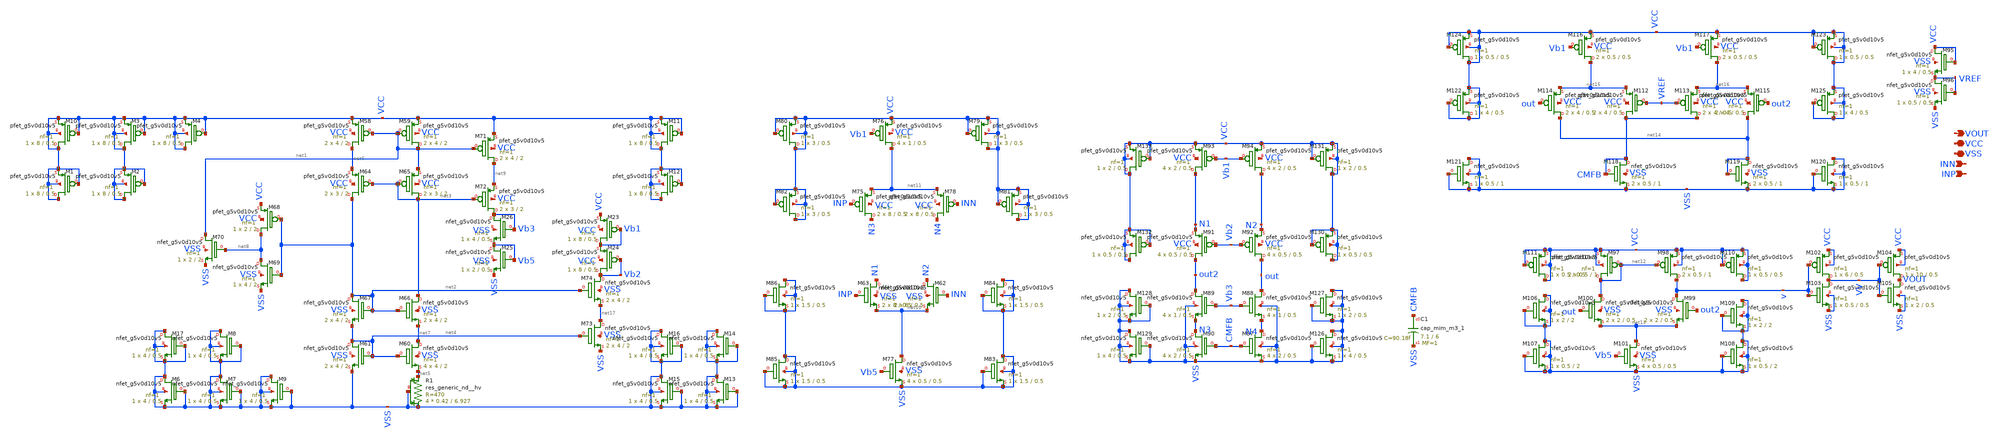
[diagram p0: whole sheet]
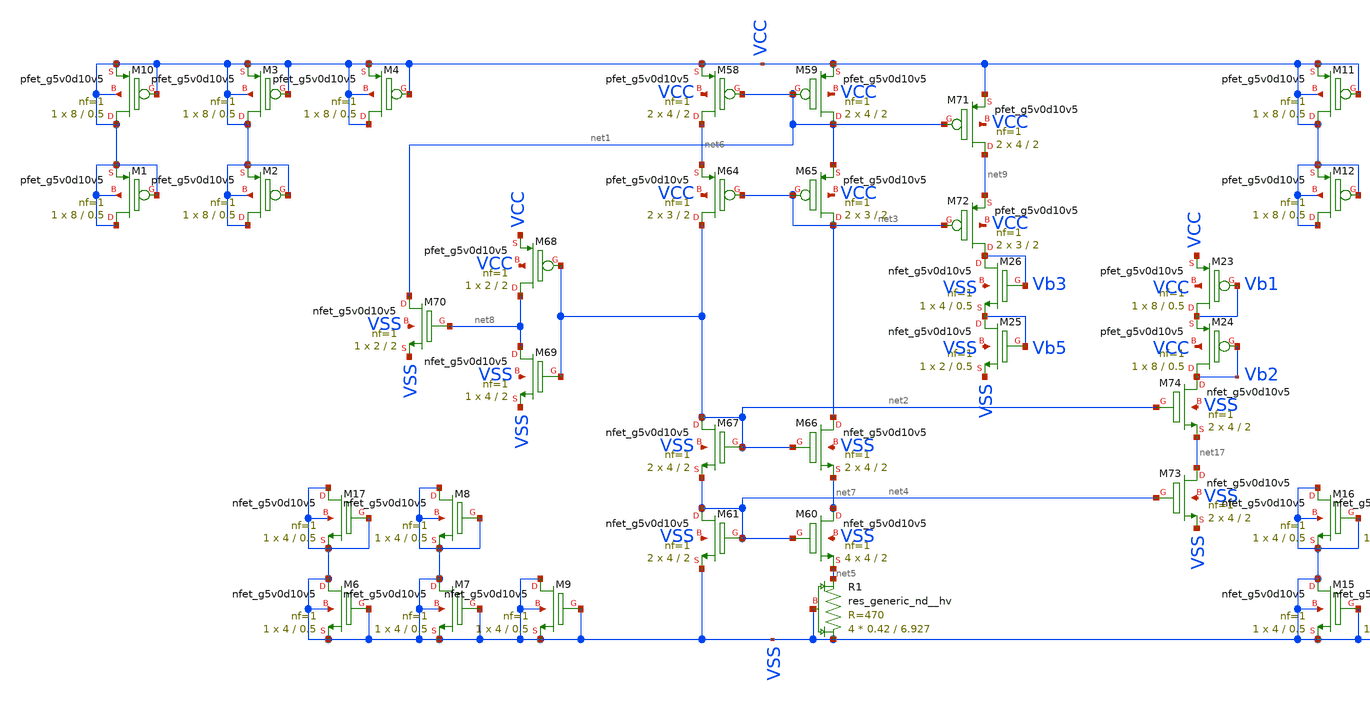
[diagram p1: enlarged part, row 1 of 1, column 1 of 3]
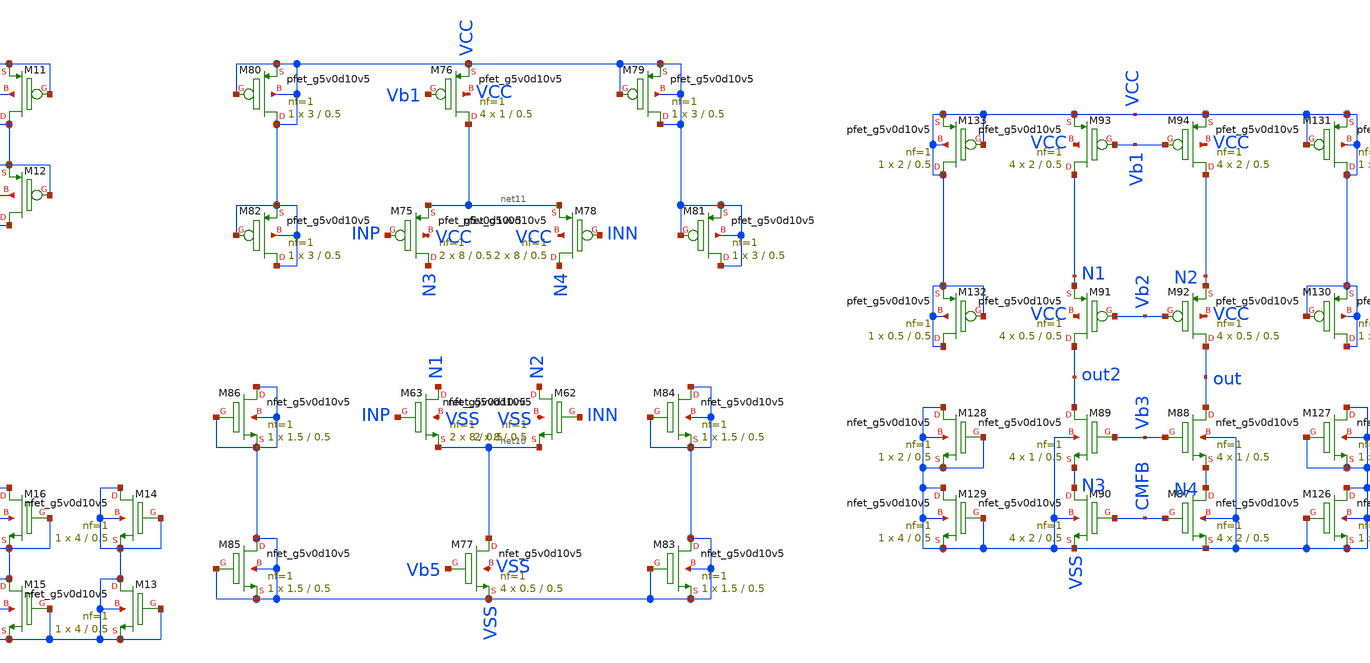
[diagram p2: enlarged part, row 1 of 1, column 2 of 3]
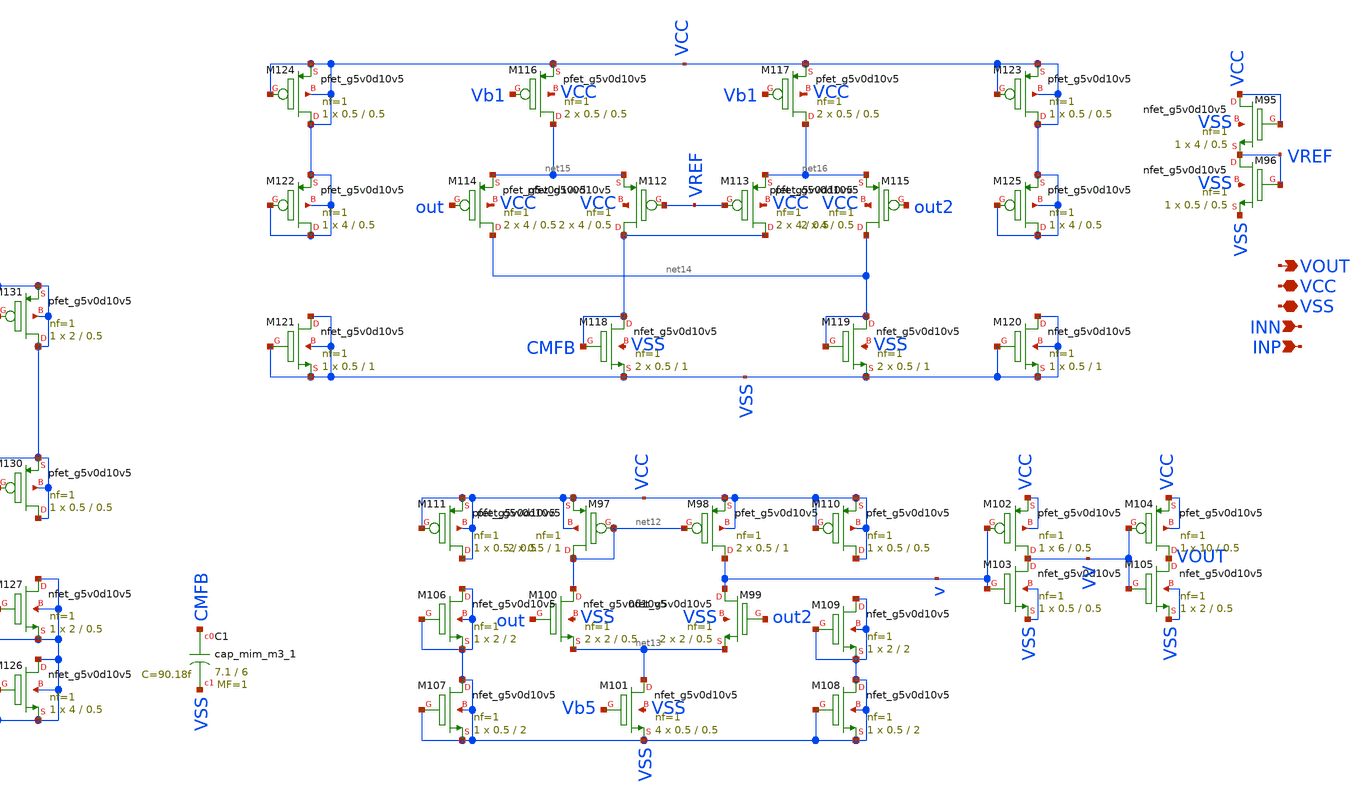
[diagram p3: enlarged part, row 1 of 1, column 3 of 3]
** sch_path: latest_working_comparator/backup_schematic/folded_cascode.sch
**.subckt folded_cascode VCC VSS INN INP VOUT
*.iopin VCC
*.iopin VSS
*.ipin INN
*.ipin INP
*.opin VOUT
XM23 Vb1 Vb1 VCC VCC sky130_fd_pr__pfet_g5v0d10v5 L=0.5 W=8 nf=1 ad='int((nf+1)/2) * W/nf * 0.29' as='int((nf+2)/2) * W/nf * 0.29'
+ pd='2*int((nf+1)/2) * (W/nf + 0.29)' ps='2*int((nf+2)/2) * (W/nf + 0.29)' nrd='0.29 / W' nrs='0.29 / W'
+ sa=0 sb=0 sd=0 mult=1 m=1
XM24 Vb2 Vb2 Vb1 VCC sky130_fd_pr__pfet_g5v0d10v5 L=0.5 W=8 nf=1 ad='int((nf+1)/2) * W/nf * 0.29' as='int((nf+2)/2) * W/nf * 0.29'
+ pd='2*int((nf+1)/2) * (W/nf + 0.29)' ps='2*int((nf+2)/2) * (W/nf + 0.29)' nrd='0.29 / W' nrs='0.29 / W'
+ sa=0 sb=0 sd=0 mult=1 m=1
XM25 Vb5 Vb5 VSS VSS sky130_fd_pr__nfet_g5v0d10v5 L=0.5 W=2 nf=1 ad='int((nf+1)/2) * W/nf * 0.29' as='int((nf+2)/2) * W/nf * 0.29'
+ pd='2*int((nf+1)/2) * (W/nf + 0.29)' ps='2*int((nf+2)/2) * (W/nf + 0.29)' nrd='0.29 / W' nrs='0.29 / W'
+ sa=0 sb=0 sd=0 mult=1 m=1
XM26 Vb3 Vb3 Vb5 VSS sky130_fd_pr__nfet_g5v0d10v5 L=0.5 W=4 nf=1 ad='int((nf+1)/2) * W/nf * 0.29' as='int((nf+2)/2) * W/nf * 0.29'
+ pd='2*int((nf+1)/2) * (W/nf + 0.29)' ps='2*int((nf+2)/2) * (W/nf + 0.29)' nrd='0.29 / W' nrs='0.29 / W'
+ sa=0 sb=0 sd=0 mult=1 m=1
XM58 net6 net1 VCC VCC sky130_fd_pr__pfet_g5v0d10v5 L=2 W=4 nf=1 ad='int((nf+1)/2) * W/nf * 0.29' as='int((nf+2)/2) * W/nf * 0.29'
+ pd='2*int((nf+1)/2) * (W/nf + 0.29)' ps='2*int((nf+2)/2) * (W/nf + 0.29)' nrd='0.29 / W' nrs='0.29 / W'
+ sa=0 sb=0 sd=0 mult=2 m=2
XM59 net1 net1 VCC VCC sky130_fd_pr__pfet_g5v0d10v5 L=2 W=4 nf=1 ad='int((nf+1)/2) * W/nf * 0.29' as='int((nf+2)/2) * W/nf * 0.29'
+ pd='2*int((nf+1)/2) * (W/nf + 0.29)' ps='2*int((nf+2)/2) * (W/nf + 0.29)' nrd='0.29 / W' nrs='0.29 / W'
+ sa=0 sb=0 sd=0 mult=2 m=2
XM60 net7 net4 net5 VSS sky130_fd_pr__nfet_g5v0d10v5 L=2 W=4 nf=1 ad='int((nf+1)/2) * W/nf * 0.29' as='int((nf+2)/2) * W/nf * 0.29'
+ pd='2*int((nf+1)/2) * (W/nf + 0.29)' ps='2*int((nf+2)/2) * (W/nf + 0.29)' nrd='0.29 / W' nrs='0.29 / W'
+ sa=0 sb=0 sd=0 mult=4 m=4
XM61 net4 net4 VSS VSS sky130_fd_pr__nfet_g5v0d10v5 L=2 W=4 nf=1 ad='int((nf+1)/2) * W/nf * 0.29' as='int((nf+2)/2) * W/nf * 0.29'
+ pd='2*int((nf+1)/2) * (W/nf + 0.29)' ps='2*int((nf+2)/2) * (W/nf + 0.29)' nrd='0.29 / W' nrs='0.29 / W'
+ sa=0 sb=0 sd=0 mult=2 m=2
XM64 net2 net3 net6 VCC sky130_fd_pr__pfet_g5v0d10v5 L=2 W=3 nf=1 ad='int((nf+1)/2) * W/nf * 0.29' as='int((nf+2)/2) * W/nf * 0.29'
+ pd='2*int((nf+1)/2) * (W/nf + 0.29)' ps='2*int((nf+2)/2) * (W/nf + 0.29)' nrd='0.29 / W' nrs='0.29 / W'
+ sa=0 sb=0 sd=0 mult=2 m=2
XM65 net3 net3 net1 VCC sky130_fd_pr__pfet_g5v0d10v5 L=2 W=3 nf=1 ad='int((nf+1)/2) * W/nf * 0.29' as='int((nf+2)/2) * W/nf * 0.29'
+ pd='2*int((nf+1)/2) * (W/nf + 0.29)' ps='2*int((nf+2)/2) * (W/nf + 0.29)' nrd='0.29 / W' nrs='0.29 / W'
+ sa=0 sb=0 sd=0 mult=2 m=2
XM66 net3 net2 net7 VSS sky130_fd_pr__nfet_g5v0d10v5 L=2 W=4 nf=1 ad='int((nf+1)/2) * W/nf * 0.29' as='int((nf+2)/2) * W/nf * 0.29'
+ pd='2*int((nf+1)/2) * (W/nf + 0.29)' ps='2*int((nf+2)/2) * (W/nf + 0.29)' nrd='0.29 / W' nrs='0.29 / W'
+ sa=0 sb=0 sd=0 mult=2 m=2
XM67 net2 net2 net4 VSS sky130_fd_pr__nfet_g5v0d10v5 L=2 W=4 nf=1 ad='int((nf+1)/2) * W/nf * 0.29' as='int((nf+2)/2) * W/nf * 0.29'
+ pd='2*int((nf+1)/2) * (W/nf + 0.29)' ps='2*int((nf+2)/2) * (W/nf + 0.29)' nrd='0.29 / W' nrs='0.29 / W'
+ sa=0 sb=0 sd=0 mult=2 m=2
XM68 net8 net2 VCC VCC sky130_fd_pr__pfet_g5v0d10v5 L=2 W=2 nf=1 ad='int((nf+1)/2) * W/nf * 0.29' as='int((nf+2)/2) * W/nf * 0.29'
+ pd='2*int((nf+1)/2) * (W/nf + 0.29)' ps='2*int((nf+2)/2) * (W/nf + 0.29)' nrd='0.29 / W' nrs='0.29 / W'
+ sa=0 sb=0 sd=0 mult=1 m=1
XM69 net8 net2 VSS VSS sky130_fd_pr__nfet_g5v0d10v5 L=2 W=4 nf=1 ad='int((nf+1)/2) * W/nf * 0.29' as='int((nf+2)/2) * W/nf * 0.29'
+ pd='2*int((nf+1)/2) * (W/nf + 0.29)' ps='2*int((nf+2)/2) * (W/nf + 0.29)' nrd='0.29 / W' nrs='0.29 / W'
+ sa=0 sb=0 sd=0 mult=1 m=1
XM70 net1 net8 VSS VSS sky130_fd_pr__nfet_g5v0d10v5 L=2 W=2 nf=1 ad='int((nf+1)/2) * W/nf * 0.29' as='int((nf+2)/2) * W/nf * 0.29'
+ pd='2*int((nf+1)/2) * (W/nf + 0.29)' ps='2*int((nf+2)/2) * (W/nf + 0.29)' nrd='0.29 / W' nrs='0.29 / W'
+ sa=0 sb=0 sd=0 mult=1 m=1
XM71 net9 net1 VCC VCC sky130_fd_pr__pfet_g5v0d10v5 L=2 W=4 nf=1 ad='int((nf+1)/2) * W/nf * 0.29' as='int((nf+2)/2) * W/nf * 0.29'
+ pd='2*int((nf+1)/2) * (W/nf + 0.29)' ps='2*int((nf+2)/2) * (W/nf + 0.29)' nrd='0.29 / W' nrs='0.29 / W'
+ sa=0 sb=0 sd=0 mult=2 m=2
XM72 Vb3 net3 net9 VCC sky130_fd_pr__pfet_g5v0d10v5 L=2 W=3 nf=1 ad='int((nf+1)/2) * W/nf * 0.29' as='int((nf+2)/2) * W/nf * 0.29'
+ pd='2*int((nf+1)/2) * (W/nf + 0.29)' ps='2*int((nf+2)/2) * (W/nf + 0.29)' nrd='0.29 / W' nrs='0.29 / W'
+ sa=0 sb=0 sd=0 mult=2 m=2
XM73 net17 net4 VSS VSS sky130_fd_pr__nfet_g5v0d10v5 L=2 W=4 nf=1 ad='int((nf+1)/2) * W/nf * 0.29' as='int((nf+2)/2) * W/nf * 0.29'
+ pd='2*int((nf+1)/2) * (W/nf + 0.29)' ps='2*int((nf+2)/2) * (W/nf + 0.29)' nrd='0.29 / W' nrs='0.29 / W'
+ sa=0 sb=0 sd=0 mult=2 m=2
XM74 Vb2 net2 net17 VSS sky130_fd_pr__nfet_g5v0d10v5 L=2 W=4 nf=1 ad='int((nf+1)/2) * W/nf * 0.29' as='int((nf+2)/2) * W/nf * 0.29'
+ pd='2*int((nf+1)/2) * (W/nf + 0.29)' ps='2*int((nf+2)/2) * (W/nf + 0.29)' nrd='0.29 / W' nrs='0.29 / W'
+ sa=0 sb=0 sd=0 mult=2 m=2
XM62 N2 INN net10 VSS sky130_fd_pr__nfet_g5v0d10v5 L=0.5 W=8 nf=1 ad='int((nf+1)/2) * W/nf * 0.29' as='int((nf+2)/2) * W/nf * 0.29'
+ pd='2*int((nf+1)/2) * (W/nf + 0.29)' ps='2*int((nf+2)/2) * (W/nf + 0.29)' nrd='0.29 / W' nrs='0.29 / W'
+ sa=0 sb=0 sd=0 mult=2 m=2
XM63 N1 INP net10 VSS sky130_fd_pr__nfet_g5v0d10v5 L=0.5 W=8 nf=1 ad='int((nf+1)/2) * W/nf * 0.29' as='int((nf+2)/2) * W/nf * 0.29'
+ pd='2*int((nf+1)/2) * (W/nf + 0.29)' ps='2*int((nf+2)/2) * (W/nf + 0.29)' nrd='0.29 / W' nrs='0.29 / W'
+ sa=0 sb=0 sd=0 mult=2 m=2
XM75 N3 INP net11 VCC sky130_fd_pr__pfet_g5v0d10v5 L=0.5 W=8 nf=1 ad='int((nf+1)/2) * W/nf * 0.29' as='int((nf+2)/2) * W/nf * 0.29'
+ pd='2*int((nf+1)/2) * (W/nf + 0.29)' ps='2*int((nf+2)/2) * (W/nf + 0.29)' nrd='0.29 / W' nrs='0.29 / W'
+ sa=0 sb=0 sd=0 mult=2 m=2
XM76 net11 Vb1 VCC VCC sky130_fd_pr__pfet_g5v0d10v5 L=0.5 W=1 nf=1 ad='int((nf+1)/2) * W/nf * 0.29' as='int((nf+2)/2) * W/nf * 0.29'
+ pd='2*int((nf+1)/2) * (W/nf + 0.29)' ps='2*int((nf+2)/2) * (W/nf + 0.29)' nrd='0.29 / W' nrs='0.29 / W'
+ sa=0 sb=0 sd=0 mult=4 m=4
XM77 net10 Vb5 VSS VSS sky130_fd_pr__nfet_g5v0d10v5 L=0.5 W=0.5 nf=1 ad='int((nf+1)/2) * W/nf * 0.29'
+ as='int((nf+2)/2) * W/nf * 0.29' pd='2*int((nf+1)/2) * (W/nf + 0.29)' ps='2*int((nf+2)/2) * (W/nf + 0.29)'
+ nrd='0.29 / W' nrs='0.29 / W' sa=0 sb=0 sd=0 mult=4 m=4
XM78 N4 INN net11 VCC sky130_fd_pr__pfet_g5v0d10v5 L=0.5 W=8 nf=1 ad='int((nf+1)/2) * W/nf * 0.29' as='int((nf+2)/2) * W/nf * 0.29'
+ pd='2*int((nf+1)/2) * (W/nf + 0.29)' ps='2*int((nf+2)/2) * (W/nf + 0.29)' nrd='0.29 / W' nrs='0.29 / W'
+ sa=0 sb=0 sd=0 mult=2 m=2
XM79 VCC VCC VCC VCC sky130_fd_pr__pfet_g5v0d10v5 L=0.5 W=3 nf=1 ad='int((nf+1)/2) * W/nf * 0.29' as='int((nf+2)/2) * W/nf * 0.29'
+ pd='2*int((nf+1)/2) * (W/nf + 0.29)' ps='2*int((nf+2)/2) * (W/nf + 0.29)' nrd='0.29 / W' nrs='0.29 / W'
+ sa=0 sb=0 sd=0 mult=1 m=1
XM80 VCC VCC VCC VCC sky130_fd_pr__pfet_g5v0d10v5 L=0.5 W=3 nf=1 ad='int((nf+1)/2) * W/nf * 0.29' as='int((nf+2)/2) * W/nf * 0.29'
+ pd='2*int((nf+1)/2) * (W/nf + 0.29)' ps='2*int((nf+2)/2) * (W/nf + 0.29)' nrd='0.29 / W' nrs='0.29 / W'
+ sa=0 sb=0 sd=0 mult=1 m=1
XM81 VCC VCC VCC VCC sky130_fd_pr__pfet_g5v0d10v5 L=0.5 W=3 nf=1 ad='int((nf+1)/2) * W/nf * 0.29' as='int((nf+2)/2) * W/nf * 0.29'
+ pd='2*int((nf+1)/2) * (W/nf + 0.29)' ps='2*int((nf+2)/2) * (W/nf + 0.29)' nrd='0.29 / W' nrs='0.29 / W'
+ sa=0 sb=0 sd=0 mult=1 m=1
XM82 VCC VCC VCC VCC sky130_fd_pr__pfet_g5v0d10v5 L=0.5 W=3 nf=1 ad='int((nf+1)/2) * W/nf * 0.29' as='int((nf+2)/2) * W/nf * 0.29'
+ pd='2*int((nf+1)/2) * (W/nf + 0.29)' ps='2*int((nf+2)/2) * (W/nf + 0.29)' nrd='0.29 / W' nrs='0.29 / W'
+ sa=0 sb=0 sd=0 mult=1 m=1
XM83 VSS VSS VSS VSS sky130_fd_pr__nfet_g5v0d10v5 L=0.5 W=1.5 nf=1 ad='int((nf+1)/2) * W/nf * 0.29' as='int((nf+2)/2) * W/nf * 0.29'
+ pd='2*int((nf+1)/2) * (W/nf + 0.29)' ps='2*int((nf+2)/2) * (W/nf + 0.29)' nrd='0.29 / W' nrs='0.29 / W'
+ sa=0 sb=0 sd=0 mult=1 m=1
XM84 VSS VSS VSS VSS sky130_fd_pr__nfet_g5v0d10v5 L=0.5 W=1.5 nf=1 ad='int((nf+1)/2) * W/nf * 0.29' as='int((nf+2)/2) * W/nf * 0.29'
+ pd='2*int((nf+1)/2) * (W/nf + 0.29)' ps='2*int((nf+2)/2) * (W/nf + 0.29)' nrd='0.29 / W' nrs='0.29 / W'
+ sa=0 sb=0 sd=0 mult=1 m=1
XM85 VSS VSS VSS VSS sky130_fd_pr__nfet_g5v0d10v5 L=0.5 W=1.5 nf=1 ad='int((nf+1)/2) * W/nf * 0.29' as='int((nf+2)/2) * W/nf * 0.29'
+ pd='2*int((nf+1)/2) * (W/nf + 0.29)' ps='2*int((nf+2)/2) * (W/nf + 0.29)' nrd='0.29 / W' nrs='0.29 / W'
+ sa=0 sb=0 sd=0 mult=1 m=1
XM86 VSS VSS VSS VSS sky130_fd_pr__nfet_g5v0d10v5 L=0.5 W=1.5 nf=1 ad='int((nf+1)/2) * W/nf * 0.29' as='int((nf+2)/2) * W/nf * 0.29'
+ pd='2*int((nf+1)/2) * (W/nf + 0.29)' ps='2*int((nf+2)/2) * (W/nf + 0.29)' nrd='0.29 / W' nrs='0.29 / W'
+ sa=0 sb=0 sd=0 mult=1 m=1
XM87 N4 CMFB VSS VSS sky130_fd_pr__nfet_g5v0d10v5 L=0.5 W=2 nf=1 ad='int((nf+1)/2) * W/nf * 0.29' as='int((nf+2)/2) * W/nf * 0.29'
+ pd='2*int((nf+1)/2) * (W/nf + 0.29)' ps='2*int((nf+2)/2) * (W/nf + 0.29)' nrd='0.29 / W' nrs='0.29 / W'
+ sa=0 sb=0 sd=0 mult=4 m=4
XM88 out Vb3 N4 VSS sky130_fd_pr__nfet_g5v0d10v5 L=0.5 W=1 nf=1 ad='int((nf+1)/2) * W/nf * 0.29' as='int((nf+2)/2) * W/nf * 0.29'
+ pd='2*int((nf+1)/2) * (W/nf + 0.29)' ps='2*int((nf+2)/2) * (W/nf + 0.29)' nrd='0.29 / W' nrs='0.29 / W'
+ sa=0 sb=0 sd=0 mult=4 m=4
XM89 out2 Vb3 N3 VSS sky130_fd_pr__nfet_g5v0d10v5 L=0.5 W=1 nf=1 ad='int((nf+1)/2) * W/nf * 0.29' as='int((nf+2)/2) * W/nf * 0.29'
+ pd='2*int((nf+1)/2) * (W/nf + 0.29)' ps='2*int((nf+2)/2) * (W/nf + 0.29)' nrd='0.29 / W' nrs='0.29 / W'
+ sa=0 sb=0 sd=0 mult=4 m=4
XM90 N3 CMFB VSS VSS sky130_fd_pr__nfet_g5v0d10v5 L=0.5 W=2 nf=1 ad='int((nf+1)/2) * W/nf * 0.29' as='int((nf+2)/2) * W/nf * 0.29'
+ pd='2*int((nf+1)/2) * (W/nf + 0.29)' ps='2*int((nf+2)/2) * (W/nf + 0.29)' nrd='0.29 / W' nrs='0.29 / W'
+ sa=0 sb=0 sd=0 mult=4 m=4
XM91 out2 Vb2 N1 VCC sky130_fd_pr__pfet_g5v0d10v5 L=0.5 W=0.5 nf=1 ad='int((nf+1)/2) * W/nf * 0.29' as='int((nf+2)/2) * W/nf * 0.29'
+ pd='2*int((nf+1)/2) * (W/nf + 0.29)' ps='2*int((nf+2)/2) * (W/nf + 0.29)' nrd='0.29 / W' nrs='0.29 / W'
+ sa=0 sb=0 sd=0 mult=4 m=4
XM92 out Vb2 N2 VCC sky130_fd_pr__pfet_g5v0d10v5 L=0.5 W=0.5 nf=1 ad='int((nf+1)/2) * W/nf * 0.29' as='int((nf+2)/2) * W/nf * 0.29'
+ pd='2*int((nf+1)/2) * (W/nf + 0.29)' ps='2*int((nf+2)/2) * (W/nf + 0.29)' nrd='0.29 / W' nrs='0.29 / W'
+ sa=0 sb=0 sd=0 mult=4 m=4
XM93 N1 Vb1 VCC VCC sky130_fd_pr__pfet_g5v0d10v5 L=0.5 W=2 nf=1 ad='int((nf+1)/2) * W/nf * 0.29' as='int((nf+2)/2) * W/nf * 0.29'
+ pd='2*int((nf+1)/2) * (W/nf + 0.29)' ps='2*int((nf+2)/2) * (W/nf + 0.29)' nrd='0.29 / W' nrs='0.29 / W'
+ sa=0 sb=0 sd=0 mult=4 m=4
XM94 N2 Vb1 VCC VCC sky130_fd_pr__pfet_g5v0d10v5 L=0.5 W=2 nf=1 ad='int((nf+1)/2) * W/nf * 0.29' as='int((nf+2)/2) * W/nf * 0.29'
+ pd='2*int((nf+1)/2) * (W/nf + 0.29)' ps='2*int((nf+2)/2) * (W/nf + 0.29)' nrd='0.29 / W' nrs='0.29 / W'
+ sa=0 sb=0 sd=0 mult=4 m=4
XM95 VCC VCC VREF VSS sky130_fd_pr__nfet_g5v0d10v5 L=0.5 W=4 nf=1 ad='int((nf+1)/2) * W/nf * 0.29' as='int((nf+2)/2) * W/nf * 0.29'
+ pd='2*int((nf+1)/2) * (W/nf + 0.29)' ps='2*int((nf+2)/2) * (W/nf + 0.29)' nrd='0.29 / W' nrs='0.29 / W'
+ sa=0 sb=0 sd=0 mult=1 m=1
XM96 VREF VREF VSS VSS sky130_fd_pr__nfet_g5v0d10v5 L=0.5 W=0.5 nf=1 ad='int((nf+1)/2) * W/nf * 0.29'
+ as='int((nf+2)/2) * W/nf * 0.29' pd='2*int((nf+1)/2) * (W/nf + 0.29)' ps='2*int((nf+2)/2) * (W/nf + 0.29)'
+ nrd='0.29 / W' nrs='0.29 / W' sa=0 sb=0 sd=0 mult=1 m=1
XM97 net12 net12 VCC VCC sky130_fd_pr__pfet_g5v0d10v5 L=1 W=0.5 nf=1 ad='int((nf+1)/2) * W/nf * 0.29'
+ as='int((nf+2)/2) * W/nf * 0.29' pd='2*int((nf+1)/2) * (W/nf + 0.29)' ps='2*int((nf+2)/2) * (W/nf + 0.29)'
+ nrd='0.29 / W' nrs='0.29 / W' sa=0 sb=0 sd=0 mult=2 m=2
XM98 v net12 VCC VCC sky130_fd_pr__pfet_g5v0d10v5 L=1 W=0.5 nf=1 ad='int((nf+1)/2) * W/nf * 0.29' as='int((nf+2)/2) * W/nf * 0.29'
+ pd='2*int((nf+1)/2) * (W/nf + 0.29)' ps='2*int((nf+2)/2) * (W/nf + 0.29)' nrd='0.29 / W' nrs='0.29 / W'
+ sa=0 sb=0 sd=0 mult=2 m=2
XM99 v out2 net13 VSS sky130_fd_pr__nfet_g5v0d10v5 L=0.5 W=2 nf=1 ad='int((nf+1)/2) * W/nf * 0.29' as='int((nf+2)/2) * W/nf * 0.29'
+ pd='2*int((nf+1)/2) * (W/nf + 0.29)' ps='2*int((nf+2)/2) * (W/nf + 0.29)' nrd='0.29 / W' nrs='0.29 / W'
+ sa=0 sb=0 sd=0 mult=2 m=2
XM100 net12 out net13 VSS sky130_fd_pr__nfet_g5v0d10v5 L=0.5 W=2 nf=1 ad='int((nf+1)/2) * W/nf * 0.29'
+ as='int((nf+2)/2) * W/nf * 0.29' pd='2*int((nf+1)/2) * (W/nf + 0.29)' ps='2*int((nf+2)/2) * (W/nf + 0.29)'
+ nrd='0.29 / W' nrs='0.29 / W' sa=0 sb=0 sd=0 mult=2 m=2
XM101 net13 Vb5 VSS VSS sky130_fd_pr__nfet_g5v0d10v5 L=0.5 W=0.5 nf=1 ad='int((nf+1)/2) * W/nf * 0.29'
+ as='int((nf+2)/2) * W/nf * 0.29' pd='2*int((nf+1)/2) * (W/nf + 0.29)' ps='2*int((nf+2)/2) * (W/nf + 0.29)'
+ nrd='0.29 / W' nrs='0.29 / W' sa=0 sb=0 sd=0 mult=4 m=4
XM102 VV v VCC VCC sky130_fd_pr__pfet_g5v0d10v5 L=0.5 W=6 nf=1 ad='int((nf+1)/2) * W/nf * 0.29' as='int((nf+2)/2) * W/nf * 0.29'
+ pd='2*int((nf+1)/2) * (W/nf + 0.29)' ps='2*int((nf+2)/2) * (W/nf + 0.29)' nrd='0.29 / W' nrs='0.29 / W'
+ sa=0 sb=0 sd=0 mult=1 m=1
XM103 VV v VSS VSS sky130_fd_pr__nfet_g5v0d10v5 L=0.5 W=0.5 nf=1 ad='int((nf+1)/2) * W/nf * 0.29' as='int((nf+2)/2) * W/nf * 0.29'
+ pd='2*int((nf+1)/2) * (W/nf + 0.29)' ps='2*int((nf+2)/2) * (W/nf + 0.29)' nrd='0.29 / W' nrs='0.29 / W'
+ sa=0 sb=0 sd=0 mult=1 m=1
XM104 VOUT VV VCC VCC sky130_fd_pr__pfet_g5v0d10v5 L=0.5 W=10 nf=1 ad='int((nf+1)/2) * W/nf * 0.29' as='int((nf+2)/2) * W/nf * 0.29'
+ pd='2*int((nf+1)/2) * (W/nf + 0.29)' ps='2*int((nf+2)/2) * (W/nf + 0.29)' nrd='0.29 / W' nrs='0.29 / W'
+ sa=0 sb=0 sd=0 mult=1 m=1
XM105 VOUT VV VSS VSS sky130_fd_pr__nfet_g5v0d10v5 L=0.5 W=2 nf=1 ad='int((nf+1)/2) * W/nf * 0.29' as='int((nf+2)/2) * W/nf * 0.29'
+ pd='2*int((nf+1)/2) * (W/nf + 0.29)' ps='2*int((nf+2)/2) * (W/nf + 0.29)' nrd='0.29 / W' nrs='0.29 / W'
+ sa=0 sb=0 sd=0 mult=1 m=1
XM106 VSS VSS VSS VSS sky130_fd_pr__nfet_g5v0d10v5 L=2 W=2 nf=1 ad='int((nf+1)/2) * W/nf * 0.29' as='int((nf+2)/2) * W/nf * 0.29'
+ pd='2*int((nf+1)/2) * (W/nf + 0.29)' ps='2*int((nf+2)/2) * (W/nf + 0.29)' nrd='0.29 / W' nrs='0.29 / W'
+ sa=0 sb=0 sd=0 mult=1 m=1
XM107 VSS VSS VSS VSS sky130_fd_pr__nfet_g5v0d10v5 L=2 W=0.5 nf=1 ad='int((nf+1)/2) * W/nf * 0.29' as='int((nf+2)/2) * W/nf * 0.29'
+ pd='2*int((nf+1)/2) * (W/nf + 0.29)' ps='2*int((nf+2)/2) * (W/nf + 0.29)' nrd='0.29 / W' nrs='0.29 / W'
+ sa=0 sb=0 sd=0 mult=1 m=1
XM108 VSS VSS VSS VSS sky130_fd_pr__nfet_g5v0d10v5 L=2 W=0.5 nf=1 ad='int((nf+1)/2) * W/nf * 0.29' as='int((nf+2)/2) * W/nf * 0.29'
+ pd='2*int((nf+1)/2) * (W/nf + 0.29)' ps='2*int((nf+2)/2) * (W/nf + 0.29)' nrd='0.29 / W' nrs='0.29 / W'
+ sa=0 sb=0 sd=0 mult=1 m=1
XM109 VSS VSS VSS VSS sky130_fd_pr__nfet_g5v0d10v5 L=2 W=2 nf=1 ad='int((nf+1)/2) * W/nf * 0.29' as='int((nf+2)/2) * W/nf * 0.29'
+ pd='2*int((nf+1)/2) * (W/nf + 0.29)' ps='2*int((nf+2)/2) * (W/nf + 0.29)' nrd='0.29 / W' nrs='0.29 / W'
+ sa=0 sb=0 sd=0 mult=1 m=1
XM110 VCC VCC VCC VCC sky130_fd_pr__pfet_g5v0d10v5 L=0.5 W=0.5 nf=1 ad='int((nf+1)/2) * W/nf * 0.29'
+ as='int((nf+2)/2) * W/nf * 0.29' pd='2*int((nf+1)/2) * (W/nf + 0.29)' ps='2*int((nf+2)/2) * (W/nf + 0.29)'
+ nrd='0.29 / W' nrs='0.29 / W' sa=0 sb=0 sd=0 mult=1 m=1
XM111 VCC VCC VCC VCC sky130_fd_pr__pfet_g5v0d10v5 L=0.5 W=0.5 nf=1 ad='int((nf+1)/2) * W/nf * 0.29'
+ as='int((nf+2)/2) * W/nf * 0.29' pd='2*int((nf+1)/2) * (W/nf + 0.29)' ps='2*int((nf+2)/2) * (W/nf + 0.29)'
+ nrd='0.29 / W' nrs='0.29 / W' sa=0 sb=0 sd=0 mult=1 m=1
XM112 CMFB VREF net15 VCC sky130_fd_pr__pfet_g5v0d10v5 L=0.5 W=4 nf=1 ad='int((nf+1)/2) * W/nf * 0.29'
+ as='int((nf+2)/2) * W/nf * 0.29' pd='2*int((nf+1)/2) * (W/nf + 0.29)' ps='2*int((nf+2)/2) * (W/nf + 0.29)'
+ nrd='0.29 / W' nrs='0.29 / W' sa=0 sb=0 sd=0 mult=2 m=2
XM113 CMFB VREF net16 VCC sky130_fd_pr__pfet_g5v0d10v5 L=0.5 W=4 nf=1 ad='int((nf+1)/2) * W/nf * 0.29'
+ as='int((nf+2)/2) * W/nf * 0.29' pd='2*int((nf+1)/2) * (W/nf + 0.29)' ps='2*int((nf+2)/2) * (W/nf + 0.29)'
+ nrd='0.29 / W' nrs='0.29 / W' sa=0 sb=0 sd=0 mult=2 m=2
XM114 net14 out net15 VCC sky130_fd_pr__pfet_g5v0d10v5 L=0.5 W=4 nf=1 ad='int((nf+1)/2) * W/nf * 0.29'
+ as='int((nf+2)/2) * W/nf * 0.29' pd='2*int((nf+1)/2) * (W/nf + 0.29)' ps='2*int((nf+2)/2) * (W/nf + 0.29)'
+ nrd='0.29 / W' nrs='0.29 / W' sa=0 sb=0 sd=0 mult=2 m=2
XM115 net14 out2 net16 VCC sky130_fd_pr__pfet_g5v0d10v5 L=0.5 W=4 nf=1 ad='int((nf+1)/2) * W/nf * 0.29'
+ as='int((nf+2)/2) * W/nf * 0.29' pd='2*int((nf+1)/2) * (W/nf + 0.29)' ps='2*int((nf+2)/2) * (W/nf + 0.29)'
+ nrd='0.29 / W' nrs='0.29 / W' sa=0 sb=0 sd=0 mult=2 m=2
XM116 net15 Vb1 VCC VCC sky130_fd_pr__pfet_g5v0d10v5 L=0.5 W=0.5 nf=1 ad='int((nf+1)/2) * W/nf * 0.29'
+ as='int((nf+2)/2) * W/nf * 0.29' pd='2*int((nf+1)/2) * (W/nf + 0.29)' ps='2*int((nf+2)/2) * (W/nf + 0.29)'
+ nrd='0.29 / W' nrs='0.29 / W' sa=0 sb=0 sd=0 mult=2 m=2
XM117 net16 Vb1 VCC VCC sky130_fd_pr__pfet_g5v0d10v5 L=0.5 W=0.5 nf=1 ad='int((nf+1)/2) * W/nf * 0.29'
+ as='int((nf+2)/2) * W/nf * 0.29' pd='2*int((nf+1)/2) * (W/nf + 0.29)' ps='2*int((nf+2)/2) * (W/nf + 0.29)'
+ nrd='0.29 / W' nrs='0.29 / W' sa=0 sb=0 sd=0 mult=2 m=2
XM118 CMFB CMFB VSS VSS sky130_fd_pr__nfet_g5v0d10v5 L=1 W=0.5 nf=1 ad='int((nf+1)/2) * W/nf * 0.29'
+ as='int((nf+2)/2) * W/nf * 0.29' pd='2*int((nf+1)/2) * (W/nf + 0.29)' ps='2*int((nf+2)/2) * (W/nf + 0.29)'
+ nrd='0.29 / W' nrs='0.29 / W' sa=0 sb=0 sd=0 mult=2 m=2
XM119 net14 net14 VSS VSS sky130_fd_pr__nfet_g5v0d10v5 L=1 W=0.5 nf=1 ad='int((nf+1)/2) * W/nf * 0.29'
+ as='int((nf+2)/2) * W/nf * 0.29' pd='2*int((nf+1)/2) * (W/nf + 0.29)' ps='2*int((nf+2)/2) * (W/nf + 0.29)'
+ nrd='0.29 / W' nrs='0.29 / W' sa=0 sb=0 sd=0 mult=2 m=2
XM120 VSS VSS VSS VSS sky130_fd_pr__nfet_g5v0d10v5 L=1 W=0.5 nf=1 ad='int((nf+1)/2) * W/nf * 0.29' as='int((nf+2)/2) * W/nf * 0.29'
+ pd='2*int((nf+1)/2) * (W/nf + 0.29)' ps='2*int((nf+2)/2) * (W/nf + 0.29)' nrd='0.29 / W' nrs='0.29 / W'
+ sa=0 sb=0 sd=0 mult=1 m=1
XM121 VSS VSS VSS VSS sky130_fd_pr__nfet_g5v0d10v5 L=1 W=0.5 nf=1 ad='int((nf+1)/2) * W/nf * 0.29' as='int((nf+2)/2) * W/nf * 0.29'
+ pd='2*int((nf+1)/2) * (W/nf + 0.29)' ps='2*int((nf+2)/2) * (W/nf + 0.29)' nrd='0.29 / W' nrs='0.29 / W'
+ sa=0 sb=0 sd=0 mult=1 m=1
XM122 VCC VCC VCC VCC sky130_fd_pr__pfet_g5v0d10v5 L=0.5 W=4 nf=1 ad='int((nf+1)/2) * W/nf * 0.29' as='int((nf+2)/2) * W/nf * 0.29'
+ pd='2*int((nf+1)/2) * (W/nf + 0.29)' ps='2*int((nf+2)/2) * (W/nf + 0.29)' nrd='0.29 / W' nrs='0.29 / W'
+ sa=0 sb=0 sd=0 mult=1 m=1
XM123 VCC VCC VCC VCC sky130_fd_pr__pfet_g5v0d10v5 L=0.5 W=0.5 nf=1 ad='int((nf+1)/2) * W/nf * 0.29'
+ as='int((nf+2)/2) * W/nf * 0.29' pd='2*int((nf+1)/2) * (W/nf + 0.29)' ps='2*int((nf+2)/2) * (W/nf + 0.29)'
+ nrd='0.29 / W' nrs='0.29 / W' sa=0 sb=0 sd=0 mult=1 m=1
XM124 VCC VCC VCC VCC sky130_fd_pr__pfet_g5v0d10v5 L=0.5 W=0.5 nf=1 ad='int((nf+1)/2) * W/nf * 0.29'
+ as='int((nf+2)/2) * W/nf * 0.29' pd='2*int((nf+1)/2) * (W/nf + 0.29)' ps='2*int((nf+2)/2) * (W/nf + 0.29)'
+ nrd='0.29 / W' nrs='0.29 / W' sa=0 sb=0 sd=0 mult=1 m=1
XM125 VCC VCC VCC VCC sky130_fd_pr__pfet_g5v0d10v5 L=0.5 W=4 nf=1 ad='int((nf+1)/2) * W/nf * 0.29' as='int((nf+2)/2) * W/nf * 0.29'
+ pd='2*int((nf+1)/2) * (W/nf + 0.29)' ps='2*int((nf+2)/2) * (W/nf + 0.29)' nrd='0.29 / W' nrs='0.29 / W'
+ sa=0 sb=0 sd=0 mult=1 m=1
XM126 VSS VSS VSS VSS sky130_fd_pr__nfet_g5v0d10v5 L=0.5 W=4 nf=1 ad='int((nf+1)/2) * W/nf * 0.29' as='int((nf+2)/2) * W/nf * 0.29'
+ pd='2*int((nf+1)/2) * (W/nf + 0.29)' ps='2*int((nf+2)/2) * (W/nf + 0.29)' nrd='0.29 / W' nrs='0.29 / W'
+ sa=0 sb=0 sd=0 mult=1 m=1
XM127 VSS VSS VSS VSS sky130_fd_pr__nfet_g5v0d10v5 L=0.5 W=2 nf=1 ad='int((nf+1)/2) * W/nf * 0.29' as='int((nf+2)/2) * W/nf * 0.29'
+ pd='2*int((nf+1)/2) * (W/nf + 0.29)' ps='2*int((nf+2)/2) * (W/nf + 0.29)' nrd='0.29 / W' nrs='0.29 / W'
+ sa=0 sb=0 sd=0 mult=1 m=1
XM128 VSS VSS VSS VSS sky130_fd_pr__nfet_g5v0d10v5 L=0.5 W=2 nf=1 ad='int((nf+1)/2) * W/nf * 0.29' as='int((nf+2)/2) * W/nf * 0.29'
+ pd='2*int((nf+1)/2) * (W/nf + 0.29)' ps='2*int((nf+2)/2) * (W/nf + 0.29)' nrd='0.29 / W' nrs='0.29 / W'
+ sa=0 sb=0 sd=0 mult=1 m=1
XM129 VSS VSS VSS VSS sky130_fd_pr__nfet_g5v0d10v5 L=0.5 W=4 nf=1 ad='int((nf+1)/2) * W/nf * 0.29' as='int((nf+2)/2) * W/nf * 0.29'
+ pd='2*int((nf+1)/2) * (W/nf + 0.29)' ps='2*int((nf+2)/2) * (W/nf + 0.29)' nrd='0.29 / W' nrs='0.29 / W'
+ sa=0 sb=0 sd=0 mult=1 m=1
XM130 VCC VCC VCC VCC sky130_fd_pr__pfet_g5v0d10v5 L=0.5 W=0.5 nf=1 ad='int((nf+1)/2) * W/nf * 0.29'
+ as='int((nf+2)/2) * W/nf * 0.29' pd='2*int((nf+1)/2) * (W/nf + 0.29)' ps='2*int((nf+2)/2) * (W/nf + 0.29)'
+ nrd='0.29 / W' nrs='0.29 / W' sa=0 sb=0 sd=0 mult=1 m=1
XM131 VCC VCC VCC VCC sky130_fd_pr__pfet_g5v0d10v5 L=0.5 W=2 nf=1 ad='int((nf+1)/2) * W/nf * 0.29' as='int((nf+2)/2) * W/nf * 0.29'
+ pd='2*int((nf+1)/2) * (W/nf + 0.29)' ps='2*int((nf+2)/2) * (W/nf + 0.29)' nrd='0.29 / W' nrs='0.29 / W'
+ sa=0 sb=0 sd=0 mult=1 m=1
XM132 VCC VCC VCC VCC sky130_fd_pr__pfet_g5v0d10v5 L=0.5 W=0.5 nf=1 ad='int((nf+1)/2) * W/nf * 0.29'
+ as='int((nf+2)/2) * W/nf * 0.29' pd='2*int((nf+1)/2) * (W/nf + 0.29)' ps='2*int((nf+2)/2) * (W/nf + 0.29)'
+ nrd='0.29 / W' nrs='0.29 / W' sa=0 sb=0 sd=0 mult=1 m=1
XM133 VCC VCC VCC VCC sky130_fd_pr__pfet_g5v0d10v5 L=0.5 W=2 nf=1 ad='int((nf+1)/2) * W/nf * 0.29' as='int((nf+2)/2) * W/nf * 0.29'
+ pd='2*int((nf+1)/2) * (W/nf + 0.29)' ps='2*int((nf+2)/2) * (W/nf + 0.29)' nrd='0.29 / W' nrs='0.29 / W'
+ sa=0 sb=0 sd=0 mult=1 m=1
XC1 CMFB VSS sky130_fd_pr__cap_mim_m3_1 W=7.1 L=6 MF=1 m=1
XM11 VCC VCC VCC VCC sky130_fd_pr__pfet_g5v0d10v5 L=0.5 W=8 nf=1 ad='int((nf+1)/2) * W/nf * 0.29' as='int((nf+2)/2) * W/nf * 0.29'
+ pd='2*int((nf+1)/2) * (W/nf + 0.29)' ps='2*int((nf+2)/2) * (W/nf + 0.29)' nrd='0.29 / W' nrs='0.29 / W'
+ sa=0 sb=0 sd=0 mult=1 m=1
XM12 VCC VCC VCC VCC sky130_fd_pr__pfet_g5v0d10v5 L=0.5 W=8 nf=1 ad='int((nf+1)/2) * W/nf * 0.29' as='int((nf+2)/2) * W/nf * 0.29'
+ pd='2*int((nf+1)/2) * (W/nf + 0.29)' ps='2*int((nf+2)/2) * (W/nf + 0.29)' nrd='0.29 / W' nrs='0.29 / W'
+ sa=0 sb=0 sd=0 mult=1 m=1
XM13 VSS VSS VSS VSS sky130_fd_pr__nfet_g5v0d10v5 L=0.5 W=4 nf=1 ad='int((nf+1)/2) * W/nf * 0.29' as='int((nf+2)/2) * W/nf * 0.29'
+ pd='2*int((nf+1)/2) * (W/nf + 0.29)' ps='2*int((nf+2)/2) * (W/nf + 0.29)' nrd='0.29 / W' nrs='0.29 / W'
+ sa=0 sb=0 sd=0 mult=1 m=1
XM14 VSS VSS VSS VSS sky130_fd_pr__nfet_g5v0d10v5 L=0.5 W=4 nf=1 ad='int((nf+1)/2) * W/nf * 0.29' as='int((nf+2)/2) * W/nf * 0.29'
+ pd='2*int((nf+1)/2) * (W/nf + 0.29)' ps='2*int((nf+2)/2) * (W/nf + 0.29)' nrd='0.29 / W' nrs='0.29 / W'
+ sa=0 sb=0 sd=0 mult=1 m=1
XM15 VSS VSS VSS VSS sky130_fd_pr__nfet_g5v0d10v5 L=0.5 W=4 nf=1 ad='int((nf+1)/2) * W/nf * 0.29' as='int((nf+2)/2) * W/nf * 0.29'
+ pd='2*int((nf+1)/2) * (W/nf + 0.29)' ps='2*int((nf+2)/2) * (W/nf + 0.29)' nrd='0.29 / W' nrs='0.29 / W'
+ sa=0 sb=0 sd=0 mult=1 m=1
XM16 VSS VSS VSS VSS sky130_fd_pr__nfet_g5v0d10v5 L=0.5 W=4 nf=1 ad='int((nf+1)/2) * W/nf * 0.29' as='int((nf+2)/2) * W/nf * 0.29'
+ pd='2*int((nf+1)/2) * (W/nf + 0.29)' ps='2*int((nf+2)/2) * (W/nf + 0.29)' nrd='0.29 / W' nrs='0.29 / W'
+ sa=0 sb=0 sd=0 mult=1 m=1
XR1 VSS net5 VSS sky130_fd_pr__res_generic_nd__hv W=0.42 L=6.927 mult=4 m=4
XM17 VSS VSS VSS VSS sky130_fd_pr__nfet_g5v0d10v5 L=0.5 W=4 nf=1 ad='int((nf+1)/2) * W/nf * 0.29' as='int((nf+2)/2) * W/nf * 0.29'
+ pd='2*int((nf+1)/2) * (W/nf + 0.29)' ps='2*int((nf+2)/2) * (W/nf + 0.29)' nrd='0.29 / W' nrs='0.29 / W'
+ sa=0 sb=0 sd=0 mult=1 m=1
XM6 VSS VSS VSS VSS sky130_fd_pr__nfet_g5v0d10v5 L=0.5 W=4 nf=1 ad='int((nf+1)/2) * W/nf * 0.29' as='int((nf+2)/2) * W/nf * 0.29'
+ pd='2*int((nf+1)/2) * (W/nf + 0.29)' ps='2*int((nf+2)/2) * (W/nf + 0.29)' nrd='0.29 / W' nrs='0.29 / W'
+ sa=0 sb=0 sd=0 mult=1 m=1
XM7 VSS VSS VSS VSS sky130_fd_pr__nfet_g5v0d10v5 L=0.5 W=4 nf=1 ad='int((nf+1)/2) * W/nf * 0.29' as='int((nf+2)/2) * W/nf * 0.29'
+ pd='2*int((nf+1)/2) * (W/nf + 0.29)' ps='2*int((nf+2)/2) * (W/nf + 0.29)' nrd='0.29 / W' nrs='0.29 / W'
+ sa=0 sb=0 sd=0 mult=1 m=1
XM8 VSS VSS VSS VSS sky130_fd_pr__nfet_g5v0d10v5 L=0.5 W=4 nf=1 ad='int((nf+1)/2) * W/nf * 0.29' as='int((nf+2)/2) * W/nf * 0.29'
+ pd='2*int((nf+1)/2) * (W/nf + 0.29)' ps='2*int((nf+2)/2) * (W/nf + 0.29)' nrd='0.29 / W' nrs='0.29 / W'
+ sa=0 sb=0 sd=0 mult=1 m=1
XM9 VSS VSS VSS VSS sky130_fd_pr__nfet_g5v0d10v5 L=0.5 W=4 nf=1 ad='int((nf+1)/2) * W/nf * 0.29' as='int((nf+2)/2) * W/nf * 0.29'
+ pd='2*int((nf+1)/2) * (W/nf + 0.29)' ps='2*int((nf+2)/2) * (W/nf + 0.29)' nrd='0.29 / W' nrs='0.29 / W'
+ sa=0 sb=0 sd=0 mult=1 m=1
XM10 VCC VCC VCC VCC sky130_fd_pr__pfet_g5v0d10v5 L=0.5 W=8 nf=1 ad='int((nf+1)/2) * W/nf * 0.29' as='int((nf+2)/2) * W/nf * 0.29'
+ pd='2*int((nf+1)/2) * (W/nf + 0.29)' ps='2*int((nf+2)/2) * (W/nf + 0.29)' nrd='0.29 / W' nrs='0.29 / W'
+ sa=0 sb=0 sd=0 mult=1 m=1
XM1 VCC VCC VCC VCC sky130_fd_pr__pfet_g5v0d10v5 L=0.5 W=8 nf=1 ad='int((nf+1)/2) * W/nf * 0.29' as='int((nf+2)/2) * W/nf * 0.29'
+ pd='2*int((nf+1)/2) * (W/nf + 0.29)' ps='2*int((nf+2)/2) * (W/nf + 0.29)' nrd='0.29 / W' nrs='0.29 / W'
+ sa=0 sb=0 sd=0 mult=1 m=1
XM2 VCC VCC VCC VCC sky130_fd_pr__pfet_g5v0d10v5 L=0.5 W=8 nf=1 ad='int((nf+1)/2) * W/nf * 0.29' as='int((nf+2)/2) * W/nf * 0.29'
+ pd='2*int((nf+1)/2) * (W/nf + 0.29)' ps='2*int((nf+2)/2) * (W/nf + 0.29)' nrd='0.29 / W' nrs='0.29 / W'
+ sa=0 sb=0 sd=0 mult=1 m=1
XM3 VCC VCC VCC VCC sky130_fd_pr__pfet_g5v0d10v5 L=0.5 W=8 nf=1 ad='int((nf+1)/2) * W/nf * 0.29' as='int((nf+2)/2) * W/nf * 0.29'
+ pd='2*int((nf+1)/2) * (W/nf + 0.29)' ps='2*int((nf+2)/2) * (W/nf + 0.29)' nrd='0.29 / W' nrs='0.29 / W'
+ sa=0 sb=0 sd=0 mult=1 m=1
XM4 VCC VCC VCC VCC sky130_fd_pr__pfet_g5v0d10v5 L=0.5 W=8 nf=1 ad='int((nf+1)/2) * W/nf * 0.29' as='int((nf+2)/2) * W/nf * 0.29'
+ pd='2*int((nf+1)/2) * (W/nf + 0.29)' ps='2*int((nf+2)/2) * (W/nf + 0.29)' nrd='0.29 / W' nrs='0.29 / W'
+ sa=0 sb=0 sd=0 mult=1 m=1
**.ends
.end
